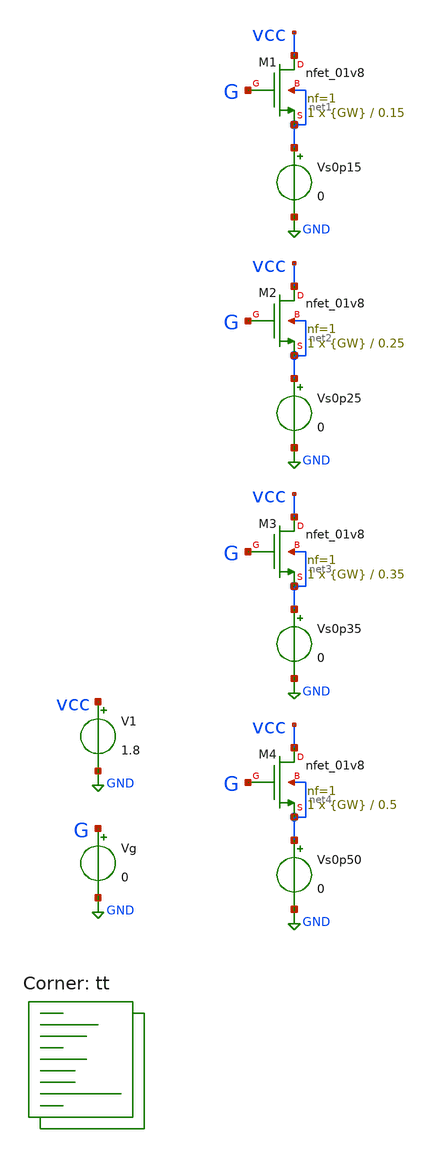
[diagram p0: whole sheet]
** sch_path: xschem/03-nfet-sweep3.sch
**.subckt 03-nfet-sweep3
XM1 vcc G net1 net1 sky130_fd_pr__nfet_01v8 L=0.15 W={GW} nf=1 ad='int((nf+1)/2) * W/nf * 0.29' as='int((nf+2)/2) * W/nf * 0.29'
+ pd='2*int((nf+1)/2) * (W/nf + 0.29)' ps='2*int((nf+2)/2) * (W/nf + 0.29)' nrd='0.29 / W' nrs='0.29 / W'
+ sa=0 sb=0 sd=0 mult=1 m=1
V1 vcc GND 1.8
Vg G GND 0
Vs0p15 net1 GND 0
XM2 vcc G net2 net2 sky130_fd_pr__nfet_01v8 L=0.25 W={GW} nf=1 ad='int((nf+1)/2) * W/nf * 0.29' as='int((nf+2)/2) * W/nf * 0.29'
+ pd='2*int((nf+1)/2) * (W/nf + 0.29)' ps='2*int((nf+2)/2) * (W/nf + 0.29)' nrd='0.29 / W' nrs='0.29 / W'
+ sa=0 sb=0 sd=0 mult=1 m=1
Vs0p25 net2 GND 0
XM3 vcc G net3 net3 sky130_fd_pr__nfet_01v8 L=0.35 W={GW} nf=1 ad='int((nf+1)/2) * W/nf * 0.29' as='int((nf+2)/2) * W/nf * 0.29'
+ pd='2*int((nf+1)/2) * (W/nf + 0.29)' ps='2*int((nf+2)/2) * (W/nf + 0.29)' nrd='0.29 / W' nrs='0.29 / W'
+ sa=0 sb=0 sd=0 mult=1 m=1
Vs0p35 net3 GND 0
XM4 vcc G net4 net4 sky130_fd_pr__nfet_01v8 L=0.5 W={GW} nf=1 ad='int((nf+1)/2) * W/nf * 0.29' as='int((nf+2)/2) * W/nf * 0.29'
+ pd='2*int((nf+1)/2) * (W/nf + 0.29)' ps='2*int((nf+2)/2) * (W/nf + 0.29)' nrd='0.29 / W' nrs='0.29 / W'
+ sa=0 sb=0 sd=0 mult=1 m=1
Vs0p50 net4 GND 0
**** begin user architecture code



.DC Vg 0 1.8 0.01

.param GW     = 0.5
.param GL     = 0.15

.options savecurrents
.control

  let gwstart = 0.5
  let gwstep  = 0.05
  let gwi     = gwstart

  repeat 10
    set gwvar=$&gwi
    echo Gate width = $gwvar
    alterparam GW = $gwvar
    save all
    run
    write 03.raw G i(Vs0p15) i(Vs0p25) i(Vs0p35) i(Vs0p50)
    set appendwrite
    reset
    let gwi = gwi + gwstep
  end

.endc



.lib $::SKYWATER_MODELS/sky130.lib.spice tt
**** end user architecture code
**.ends
.GLOBAL GND
.end
